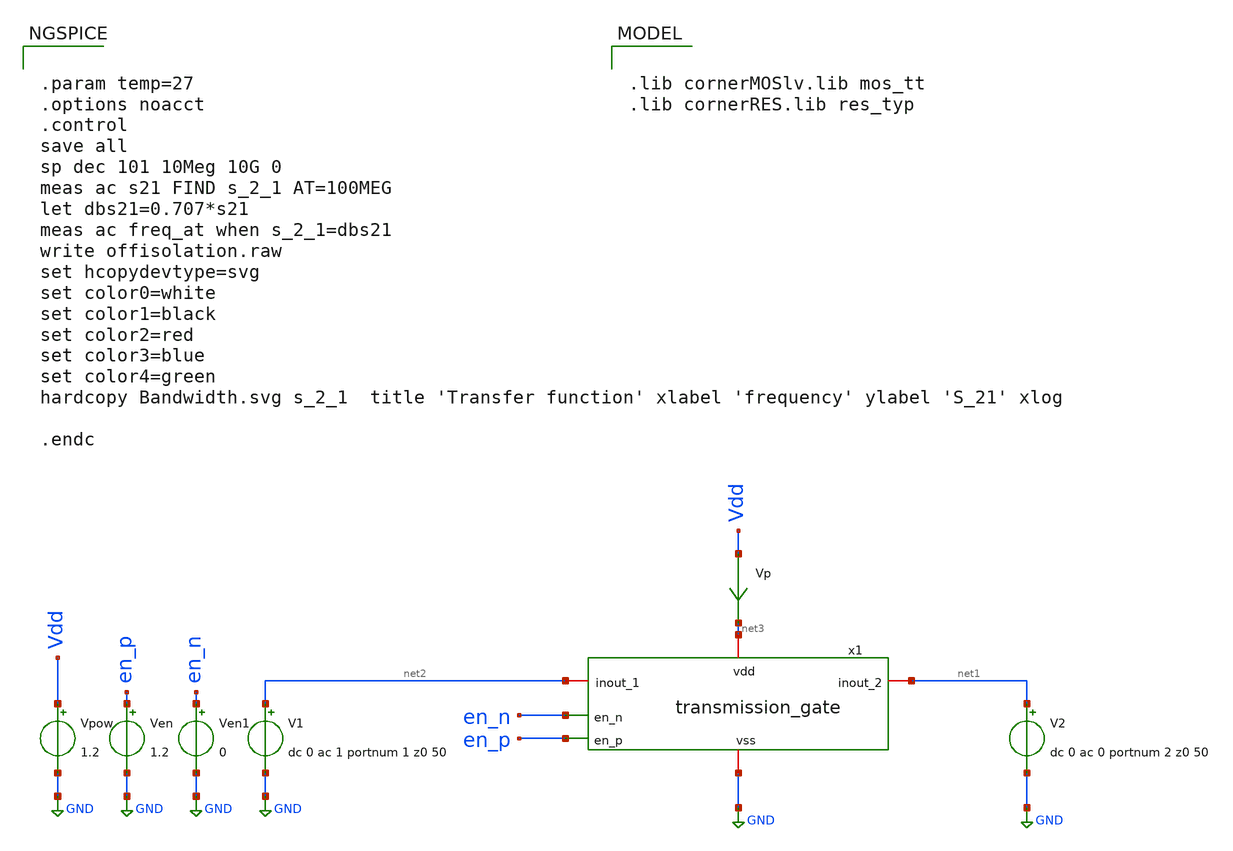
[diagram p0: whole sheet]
** sch_path: CHIPCHILE_CANELOS24_WorkshopTO/design_data/xschem/tgate/transmission_gate_tb_Bandwidth.sch
* Copyright 2023 IHP PDK Authors
**.subckt transmission_gate_tb_Bandwidth
Vpow Vdd GND 1.2
Vp Vdd net3 0
.save i(vp)
Ven en_p GND 1.2
Ven1 en_n GND 0
x1 net3 en_n net2 net1 en_p GND transmission_gate
V1 net2 GND dc 0 ac 1 portnum 1 z0 50
V2 net1 GND dc 0 ac 0 portnum 2 z0 50
**** begin user architecture code

.lib cornerMOSlv.lib mos_tt
.lib cornerRES.lib res_typ



.param temp=27
.options noacct
.control
save all
sp dec 101 10Meg 10G 0
meas ac s21 FIND s_2_1 AT=100MEG
let dbs21=0.707*s21
meas ac freq_at when s_2_1=dbs21
write offisolation.raw
set hcopydevtype=svg
set color0=white
set color1=black
set color2=red
set color3=blue
set color4=green
hardcopy Bandwidth.svg s_2_1  title 'Transfer function' xlabel 'frequency' ylabel 'S_21' xlog

.endc


**** end user architecture code
**.ends

* expanding   symbol:  transmission_gate.sym # of pins=6
** sym_path: CHIPCHILE_CANELOS24_WorkshopTO/design_data/xschem/multiplexer/transmission_gate.sym
** sch_path: CHIPCHILE_CANELOS24_WorkshopTO/design_data/xschem/multiplexer/transmission_gate.sch
.subckt transmission_gate vdd en_n inout_1 inout_2 en_p vss
*.iopin inout_1
*.iopin inout_2
*.ipin en_p
*.iopin vdd
*.iopin vss
*.ipin en_n
XM1 inout_1 en_p inout_2 net1 sg13_lv_nmos w=200.0u l=0.130u ng=20 m=1 mm_ok=1
XM2 inout_1 en_n inout_2 net2 sg13_lv_pmos w=200.0u l=0.130u ng=20 m=1 mm_ok=1
XR1 vdd net2 ntap1 R=262.8 w=0.78e-6 l=0.78e-6
XR2 vss net1 ptap1 R=262.8 w=0.78e-6 l=0.78e-6
.ends

.GLOBAL GND
.end
